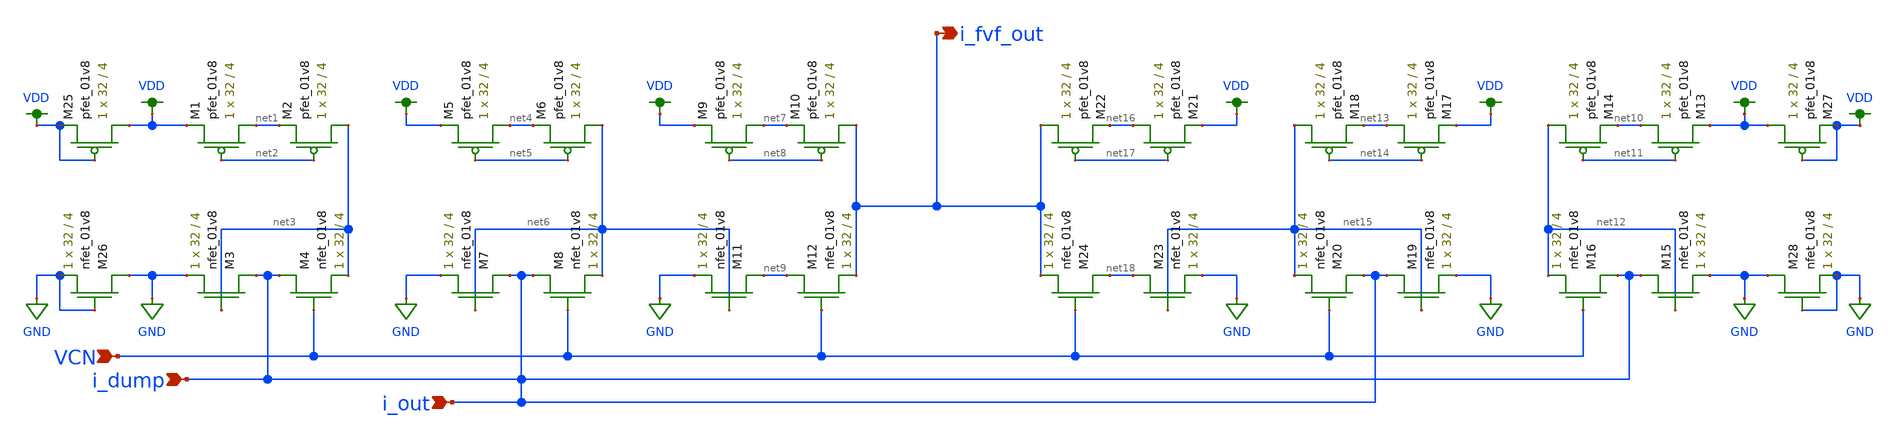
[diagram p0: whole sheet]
** sch_path: schemas/LDS_FVF_BLOCK.sch
**.subckt LDS_FVF_BLOCK i_fvf_out i_dump i_out VCN
*.opin i_fvf_out
*.ipin i_dump
*.ipin i_out
*.ipin VCN
XM1 net1 net2 VDD VDD sky130_fd_pr__pfet_01v8 L=4 W=32 nf=1 ad='int((nf+1)/2) * W/nf * 0.29' as='int((nf+2)/2) * W/nf * 0.29'
+ pd='2*int((nf+1)/2) * (W/nf + 0.29)' ps='2*int((nf+2)/2) * (W/nf + 0.29)' nrd='0.29 / W' nrs='0.29 / W'
+ sa=0 sb=0 sd=0 mult=1 m=1
XM2 net3 net2 net1 VDD sky130_fd_pr__pfet_01v8 L=4 W=32 nf=1 ad='int((nf+1)/2) * W/nf * 0.29' as='int((nf+2)/2) * W/nf * 0.29'
+ pd='2*int((nf+1)/2) * (W/nf + 0.29)' ps='2*int((nf+2)/2) * (W/nf + 0.29)' nrd='0.29 / W' nrs='0.29 / W'
+ sa=0 sb=0 sd=0 mult=1 m=1
XM3 i_dump net3 GND GND sky130_fd_pr__nfet_01v8 L=4 W=32 nf=1 ad='int((nf+1)/2) * W/nf * 0.29' as='int((nf+2)/2) * W/nf * 0.29'
+ pd='2*int((nf+1)/2) * (W/nf + 0.29)' ps='2*int((nf+2)/2) * (W/nf + 0.29)' nrd='0.29 / W' nrs='0.29 / W'
+ sa=0 sb=0 sd=0 mult=1 m=1
XM4 i_dump VCN net3 GND sky130_fd_pr__nfet_01v8 L=4 W=32 nf=1 ad='int((nf+1)/2) * W/nf * 0.29' as='int((nf+2)/2) * W/nf * 0.29'
+ pd='2*int((nf+1)/2) * (W/nf + 0.29)' ps='2*int((nf+2)/2) * (W/nf + 0.29)' nrd='0.29 / W' nrs='0.29 / W'
+ sa=0 sb=0 sd=0 mult=1 m=1
XM5 net4 net5 VDD VDD sky130_fd_pr__pfet_01v8 L=4 W=32 nf=1 ad='int((nf+1)/2) * W/nf * 0.29' as='int((nf+2)/2) * W/nf * 0.29'
+ pd='2*int((nf+1)/2) * (W/nf + 0.29)' ps='2*int((nf+2)/2) * (W/nf + 0.29)' nrd='0.29 / W' nrs='0.29 / W'
+ sa=0 sb=0 sd=0 mult=1 m=1
XM6 net6 net5 net4 VDD sky130_fd_pr__pfet_01v8 L=4 W=32 nf=1 ad='int((nf+1)/2) * W/nf * 0.29' as='int((nf+2)/2) * W/nf * 0.29'
+ pd='2*int((nf+1)/2) * (W/nf + 0.29)' ps='2*int((nf+2)/2) * (W/nf + 0.29)' nrd='0.29 / W' nrs='0.29 / W'
+ sa=0 sb=0 sd=0 mult=1 m=1
XM7 i_dump net6 GND GND sky130_fd_pr__nfet_01v8 L=4 W=32 nf=1 ad='int((nf+1)/2) * W/nf * 0.29' as='int((nf+2)/2) * W/nf * 0.29'
+ pd='2*int((nf+1)/2) * (W/nf + 0.29)' ps='2*int((nf+2)/2) * (W/nf + 0.29)' nrd='0.29 / W' nrs='0.29 / W'
+ sa=0 sb=0 sd=0 mult=1 m=1
XM8 i_dump VCN net6 GND sky130_fd_pr__nfet_01v8 L=4 W=32 nf=1 ad='int((nf+1)/2) * W/nf * 0.29' as='int((nf+2)/2) * W/nf * 0.29'
+ pd='2*int((nf+1)/2) * (W/nf + 0.29)' ps='2*int((nf+2)/2) * (W/nf + 0.29)' nrd='0.29 / W' nrs='0.29 / W'
+ sa=0 sb=0 sd=0 mult=1 m=1
XM9 net7 net8 VDD VDD sky130_fd_pr__pfet_01v8 L=4 W=32 nf=1 ad='int((nf+1)/2) * W/nf * 0.29' as='int((nf+2)/2) * W/nf * 0.29'
+ pd='2*int((nf+1)/2) * (W/nf + 0.29)' ps='2*int((nf+2)/2) * (W/nf + 0.29)' nrd='0.29 / W' nrs='0.29 / W'
+ sa=0 sb=0 sd=0 mult=1 m=1
XM10 i_fvf_out net8 net7 VDD sky130_fd_pr__pfet_01v8 L=4 W=32 nf=1 ad='int((nf+1)/2) * W/nf * 0.29' as='int((nf+2)/2) * W/nf * 0.29'
+ pd='2*int((nf+1)/2) * (W/nf + 0.29)' ps='2*int((nf+2)/2) * (W/nf + 0.29)' nrd='0.29 / W' nrs='0.29 / W'
+ sa=0 sb=0 sd=0 mult=1 m=1
XM11 net9 net6 GND GND sky130_fd_pr__nfet_01v8 L=4 W=32 nf=1 ad='int((nf+1)/2) * W/nf * 0.29' as='int((nf+2)/2) * W/nf * 0.29'
+ pd='2*int((nf+1)/2) * (W/nf + 0.29)' ps='2*int((nf+2)/2) * (W/nf + 0.29)' nrd='0.29 / W' nrs='0.29 / W'
+ sa=0 sb=0 sd=0 mult=1 m=1
XM12 net9 VCN i_fvf_out GND sky130_fd_pr__nfet_01v8 L=4 W=32 nf=1 ad='int((nf+1)/2) * W/nf * 0.29' as='int((nf+2)/2) * W/nf * 0.29'
+ pd='2*int((nf+1)/2) * (W/nf + 0.29)' ps='2*int((nf+2)/2) * (W/nf + 0.29)' nrd='0.29 / W' nrs='0.29 / W'
+ sa=0 sb=0 sd=0 mult=1 m=1
XM13 net10 net11 VDD VDD sky130_fd_pr__pfet_01v8 L=4 W=32 nf=1 ad='int((nf+1)/2) * W/nf * 0.29' as='int((nf+2)/2) * W/nf * 0.29'
+ pd='2*int((nf+1)/2) * (W/nf + 0.29)' ps='2*int((nf+2)/2) * (W/nf + 0.29)' nrd='0.29 / W' nrs='0.29 / W'
+ sa=0 sb=0 sd=0 mult=1 m=1
XM14 net12 net11 net10 VDD sky130_fd_pr__pfet_01v8 L=4 W=32 nf=1 ad='int((nf+1)/2) * W/nf * 0.29' as='int((nf+2)/2) * W/nf * 0.29'
+ pd='2*int((nf+1)/2) * (W/nf + 0.29)' ps='2*int((nf+2)/2) * (W/nf + 0.29)' nrd='0.29 / W' nrs='0.29 / W'
+ sa=0 sb=0 sd=0 mult=1 m=1
XM15 i_dump net12 GND GND sky130_fd_pr__nfet_01v8 L=4 W=32 nf=1 ad='int((nf+1)/2) * W/nf * 0.29' as='int((nf+2)/2) * W/nf * 0.29'
+ pd='2*int((nf+1)/2) * (W/nf + 0.29)' ps='2*int((nf+2)/2) * (W/nf + 0.29)' nrd='0.29 / W' nrs='0.29 / W'
+ sa=0 sb=0 sd=0 mult=1 m=1
XM16 i_dump VCN net12 GND sky130_fd_pr__nfet_01v8 L=4 W=32 nf=1 ad='int((nf+1)/2) * W/nf * 0.29' as='int((nf+2)/2) * W/nf * 0.29'
+ pd='2*int((nf+1)/2) * (W/nf + 0.29)' ps='2*int((nf+2)/2) * (W/nf + 0.29)' nrd='0.29 / W' nrs='0.29 / W'
+ sa=0 sb=0 sd=0 mult=1 m=1
XM17 net13 net14 VDD VDD sky130_fd_pr__pfet_01v8 L=4 W=32 nf=1 ad='int((nf+1)/2) * W/nf * 0.29' as='int((nf+2)/2) * W/nf * 0.29'
+ pd='2*int((nf+1)/2) * (W/nf + 0.29)' ps='2*int((nf+2)/2) * (W/nf + 0.29)' nrd='0.29 / W' nrs='0.29 / W'
+ sa=0 sb=0 sd=0 mult=1 m=1
XM18 net15 net14 net13 VDD sky130_fd_pr__pfet_01v8 L=4 W=32 nf=1 ad='int((nf+1)/2) * W/nf * 0.29' as='int((nf+2)/2) * W/nf * 0.29'
+ pd='2*int((nf+1)/2) * (W/nf + 0.29)' ps='2*int((nf+2)/2) * (W/nf + 0.29)' nrd='0.29 / W' nrs='0.29 / W'
+ sa=0 sb=0 sd=0 mult=1 m=1
XM19 i_dump net15 GND GND sky130_fd_pr__nfet_01v8 L=4 W=32 nf=1 ad='int((nf+1)/2) * W/nf * 0.29' as='int((nf+2)/2) * W/nf * 0.29'
+ pd='2*int((nf+1)/2) * (W/nf + 0.29)' ps='2*int((nf+2)/2) * (W/nf + 0.29)' nrd='0.29 / W' nrs='0.29 / W'
+ sa=0 sb=0 sd=0 mult=1 m=1
XM20 i_dump VCN net15 GND sky130_fd_pr__nfet_01v8 L=4 W=32 nf=1 ad='int((nf+1)/2) * W/nf * 0.29' as='int((nf+2)/2) * W/nf * 0.29'
+ pd='2*int((nf+1)/2) * (W/nf + 0.29)' ps='2*int((nf+2)/2) * (W/nf + 0.29)' nrd='0.29 / W' nrs='0.29 / W'
+ sa=0 sb=0 sd=0 mult=1 m=1
XM21 net16 net17 VDD VDD sky130_fd_pr__pfet_01v8 L=4 W=32 nf=1 ad='int((nf+1)/2) * W/nf * 0.29' as='int((nf+2)/2) * W/nf * 0.29'
+ pd='2*int((nf+1)/2) * (W/nf + 0.29)' ps='2*int((nf+2)/2) * (W/nf + 0.29)' nrd='0.29 / W' nrs='0.29 / W'
+ sa=0 sb=0 sd=0 mult=1 m=1
XM22 i_fvf_out net17 net16 VDD sky130_fd_pr__pfet_01v8 L=4 W=32 nf=1 ad='int((nf+1)/2) * W/nf * 0.29'
+ as='int((nf+2)/2) * W/nf * 0.29' pd='2*int((nf+1)/2) * (W/nf + 0.29)' ps='2*int((nf+2)/2) * (W/nf + 0.29)'
+ nrd='0.29 / W' nrs='0.29 / W' sa=0 sb=0 sd=0 mult=1 m=1
XM23 net18 net15 GND GND sky130_fd_pr__nfet_01v8 L=4 W=32 nf=1 ad='int((nf+1)/2) * W/nf * 0.29' as='int((nf+2)/2) * W/nf * 0.29'
+ pd='2*int((nf+1)/2) * (W/nf + 0.29)' ps='2*int((nf+2)/2) * (W/nf + 0.29)' nrd='0.29 / W' nrs='0.29 / W'
+ sa=0 sb=0 sd=0 mult=1 m=1
XM24 net18 VCN i_fvf_out GND sky130_fd_pr__nfet_01v8 L=4 W=32 nf=1 ad='int((nf+1)/2) * W/nf * 0.29' as='int((nf+2)/2) * W/nf * 0.29'
+ pd='2*int((nf+1)/2) * (W/nf + 0.29)' ps='2*int((nf+2)/2) * (W/nf + 0.29)' nrd='0.29 / W' nrs='0.29 / W'
+ sa=0 sb=0 sd=0 mult=1 m=1
XM25 VDD VDD VDD VDD sky130_fd_pr__pfet_01v8 L=4 W=32 nf=1 ad='int((nf+1)/2) * W/nf * 0.29' as='int((nf+2)/2) * W/nf * 0.29'
+ pd='2*int((nf+1)/2) * (W/nf + 0.29)' ps='2*int((nf+2)/2) * (W/nf + 0.29)' nrd='0.29 / W' nrs='0.29 / W'
+ sa=0 sb=0 sd=0 mult=1 m=1
XM26 GND GND GND GND sky130_fd_pr__nfet_01v8 L=4 W=32 nf=1 ad='int((nf+1)/2) * W/nf * 0.29' as='int((nf+2)/2) * W/nf * 0.29'
+ pd='2*int((nf+1)/2) * (W/nf + 0.29)' ps='2*int((nf+2)/2) * (W/nf + 0.29)' nrd='0.29 / W' nrs='0.29 / W'
+ sa=0 sb=0 sd=0 mult=1 m=1
XM27 VDD VDD VDD VDD sky130_fd_pr__pfet_01v8 L=4 W=32 nf=1 ad='int((nf+1)/2) * W/nf * 0.29' as='int((nf+2)/2) * W/nf * 0.29'
+ pd='2*int((nf+1)/2) * (W/nf + 0.29)' ps='2*int((nf+2)/2) * (W/nf + 0.29)' nrd='0.29 / W' nrs='0.29 / W'
+ sa=0 sb=0 sd=0 mult=1 m=1
XM28 GND GND GND GND sky130_fd_pr__nfet_01v8 L=4 W=32 nf=1 ad='int((nf+1)/2) * W/nf * 0.29' as='int((nf+2)/2) * W/nf * 0.29'
+ pd='2*int((nf+1)/2) * (W/nf + 0.29)' ps='2*int((nf+2)/2) * (W/nf + 0.29)' nrd='0.29 / W' nrs='0.29 / W'
+ sa=0 sb=0 sd=0 mult=1 m=1
**.ends
.GLOBAL GND
.GLOBAL VDD
.end
